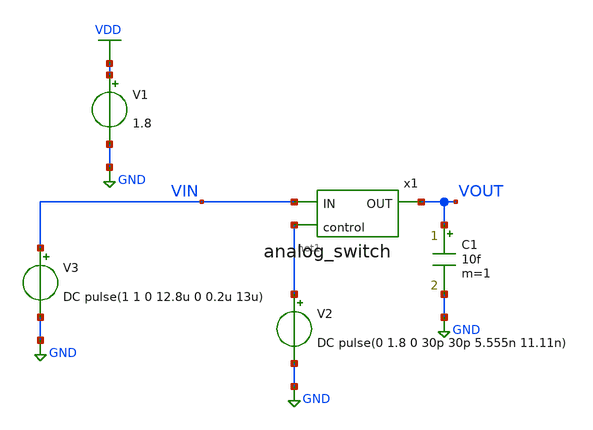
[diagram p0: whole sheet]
** sch_path: xschem/tb_switch.sch
* Copyright 2021 Stefan Frederik Schippers
* Licensed under the Apache License, Version 2.0 (the "License");
* you may not use this file except in compliance with the License.
* You may obtain a copy of the License at
* https://www.apache.org/licenses/LICENSE-2.0
* Unless required by applicable law or agreed to in writing, software
* distributed under the License is distributed on an "AS IS" BASIS,
* WITHOUT WARRANTIES OR CONDITIONS OF ANY KIND, either express or implied.
* See the License for the specific language governing permissions and
* limitations under the License.
**.subckt tb_switch
V2 net1 GND DC pulse(0 1.8 0 30p 30p 5.555n 11.11n)
V3 VIN GND DC pulse(1 1 0 12.8u 0 0.2u 13u)
V1 VDD GND 1.8
x1 net1 VOUT VIN analog_switch
C1 VOUT GND 10f m=1
**** begin user architecture code
 .lib $::SKYWATER_MODELS/sky130.lib.spice tt
.include $::SKYWATER_STDCELLS/sky130_fd_sc_hd.spice



.options acct list
.temp 25
.control
tran 10n 13u
write tb_saradc.raw
plot VIN VOUT
.endc


**** end user architecture code
**.ends

* expanding   symbol:  analog_switch.sym # of pins=3
** sym_path: xschem/analog_switch.sym
** sch_path: xschem/analog_switch.sch
.subckt analog_switch control OUT IN
*.ipin IN
*.ipin control
*.opin OUT
x1 net1 OUT IN control transmission_gate
x2 control net1 not
.ends


* expanding   symbol:  transmission_gate.sym # of pins=4
** sym_path: xschem/transmission_gate.sym
** sch_path: xschem/transmission_gate.sch
.subckt transmission_gate GP OUT IN GN
*.opin OUT
*.ipin IN
*.ipin GN
*.ipin GP
XM1 OUT GN IN GND sky130_fd_pr__nfet_01v8_lvt L=0.15 W=1 nf=1 ad='int((nf+1)/2) * W/nf * 0.29' as='int((nf+2)/2) * W/nf * 0.29'
+ pd='2*int((nf+1)/2) * (W/nf + 0.29)' ps='2*int((nf+2)/2) * (W/nf + 0.29)' nrd='0.29 / W' nrs='0.29 / W'
+ sa=0 sb=0 sd=0 mult=1 m=1
XM2 OUT GP IN VDD sky130_fd_pr__pfet_01v8_lvt L=0.35 W=1 nf=1 ad='int((nf+1)/2) * W/nf * 0.29' as='int((nf+2)/2) * W/nf * 0.29'
+ pd='2*int((nf+1)/2) * (W/nf + 0.29)' ps='2*int((nf+2)/2) * (W/nf + 0.29)' nrd='0.29 / W' nrs='0.29 / W'
+ sa=0 sb=0 sd=0 mult=1 m=1
.ends


* expanding   symbol:  not.sym # of pins=2
** sym_path: xschem/not.sym
** sch_path: xschem/not.sch
.subckt not a y
*.ipin a
*.opin y
XM1 y a GND GND sky130_fd_pr__nfet_01v8_lvt L=0.15 W=1 nf=1 ad='int((nf+1)/2) * W/nf * 0.29' as='int((nf+2)/2) * W/nf * 0.29'
+ pd='2*int((nf+1)/2) * (W/nf + 0.29)' ps='2*int((nf+2)/2) * (W/nf + 0.29)' nrd='0.29 / W' nrs='0.29 / W'
+ sa=0 sb=0 sd=0 mult=1 m=1
XM2 y a VDD VDD sky130_fd_pr__pfet_01v8_lvt L=0.35 W=1 nf=1 ad='int((nf+1)/2) * W/nf * 0.29' as='int((nf+2)/2) * W/nf * 0.29'
+ pd='2*int((nf+1)/2) * (W/nf + 0.29)' ps='2*int((nf+2)/2) * (W/nf + 0.29)' nrd='0.29 / W' nrs='0.29 / W'
+ sa=0 sb=0 sd=0 mult=1 m=1
.ends

.GLOBAL GND
.GLOBAL VDD
.end
